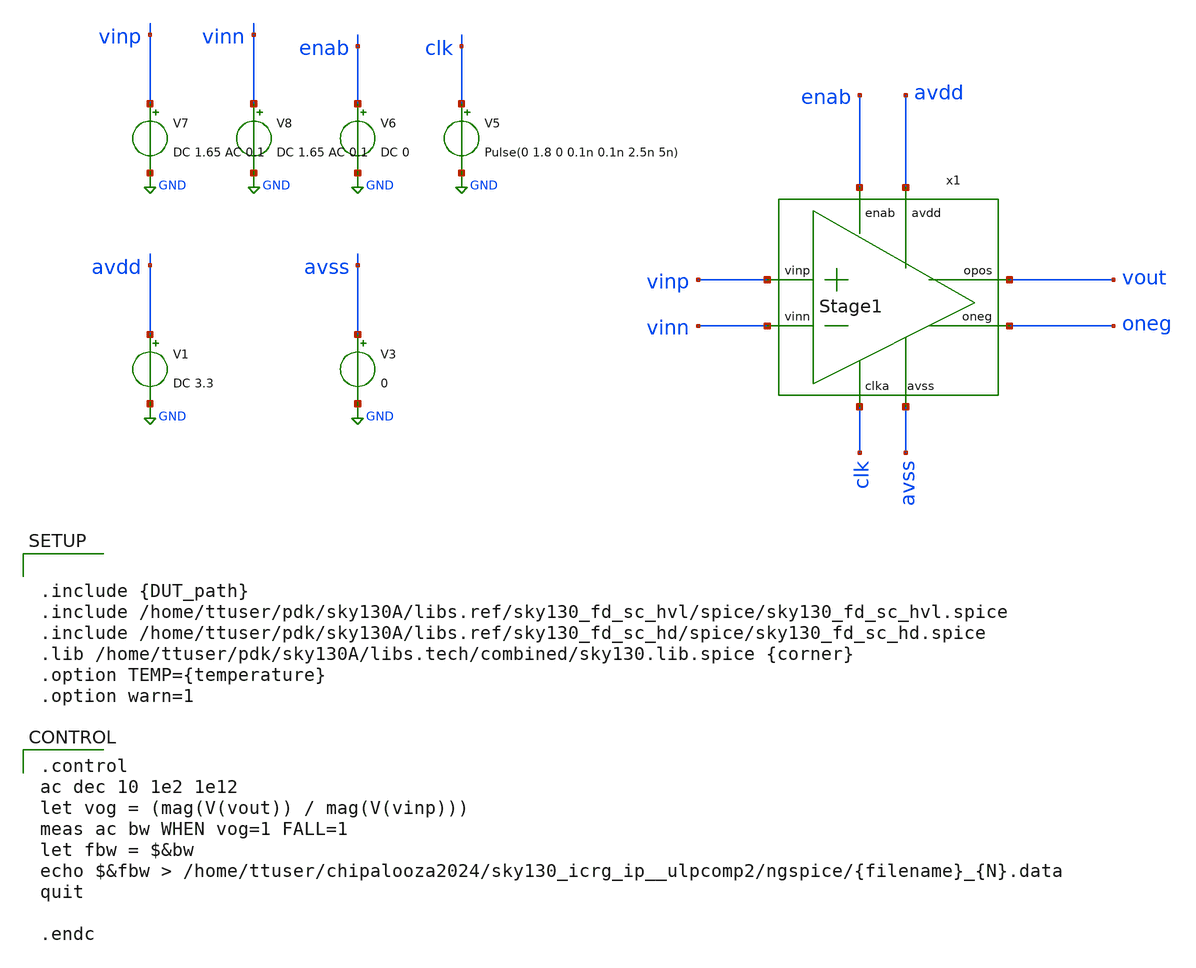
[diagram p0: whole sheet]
** sch_path: cace/fbw.sch
**.subckt fbw
V1 avdd GND DC 3.3
V3 avss GND 0
V5 clk GND Pulse(0 1.8 0 0.1n 0.1n 2.5n 5n)
V6 enab GND DC 0
V7 vinp GND DC 1.65 AC 0.1
V8 vinn GND DC 1.65 AC 0.1
x1 avdd enab clk vinn vinp oneg vout avss Stage1
**** begin user architecture code


.include {DUT_path}
.include /home/ttuser/pdk/sky130A/libs.ref/sky130_fd_sc_hvl/spice/sky130_fd_sc_hvl.spice
.include /home/ttuser/pdk/sky130A/libs.ref/sky130_fd_sc_hd/spice/sky130_fd_sc_hd.spice
.lib /home/ttuser/pdk/sky130A/libs.tech/combined/sky130.lib.spice {corner}
.option TEMP={temperature}
.option warn=1


.control
ac dec 10 1e2 1e12
let vog = (mag(V(vout)) / mag(V(vinp)))
meas ac bw WHEN vog=1 FALL=1
let fbw = $&bw
echo $&fbw > /home/ttuser/chipalooza2024/sky130_icrg_ip__ulpcomp2/ngspice/{filename}_{N}.data
quit

.endc

**** end user architecture code
**.ends

* expanding   symbol:  Stage1.sym # of pins=8
** sym_path: xschem/Stage1.sym
** sch_path: xschem/Stage1.sch
.subckt Stage1 avdd enab clka vinn vinp oneg opos avss
*.ipin avdd
*.ipin vinp
*.ipin vinn
*.opin avss
*.ipin clka
*.opin opos
*.opin oneg
*.ipin enab
XM2 oneg vinp net1 net1 sky130_fd_pr__pfet_g5v0d10v5 L=1 W=5 nf=1 ad='int((nf+1)/2) * W/nf * 0.29' as='int((nf+2)/2) * W/nf * 0.29'
+ pd='2*int((nf+1)/2) * (W/nf + 0.29)' ps='2*int((nf+2)/2) * (W/nf + 0.29)' nrd='0.29 / W' nrs='0.29 / W'
+ sa=0 sb=0 sd=0 mult=1 m=1
XM3 opos vinn net1 net1 sky130_fd_pr__pfet_g5v0d10v5 L=1 W=5 nf=1 ad='int((nf+1)/2) * W/nf * 0.29' as='int((nf+2)/2) * W/nf * 0.29'
+ pd='2*int((nf+1)/2) * (W/nf + 0.29)' ps='2*int((nf+2)/2) * (W/nf + 0.29)' nrd='0.29 / W' nrs='0.29 / W'
+ sa=0 sb=0 sd=0 mult=1 m=1
XM7 oneg clka net2 net2 sky130_fd_pr__nfet_03v3_nvt L=0.5 W=3 nf=1 ad='int((nf+1)/2) * W/nf * 0.29' as='int((nf+2)/2) * W/nf * 0.29'
+ pd='2*int((nf+1)/2) * (W/nf + 0.29)' ps='2*int((nf+2)/2) * (W/nf + 0.29)' nrd='0.29 / W' nrs='0.29 / W'
+ sa=0 sb=0 sd=0 mult=1 m=1
XM5 opos clka net2 net2 sky130_fd_pr__nfet_03v3_nvt L=0.5 W=3 nf=1 ad='int((nf+1)/2) * W/nf * 0.29' as='int((nf+2)/2) * W/nf * 0.29'
+ pd='2*int((nf+1)/2) * (W/nf + 0.29)' ps='2*int((nf+2)/2) * (W/nf + 0.29)' nrd='0.29 / W' nrs='0.29 / W'
+ sa=0 sb=0 sd=0 mult=1 m=1
XM4 net2 net2 avss avss sky130_fd_pr__nfet_03v3_nvt L=0.5 W=3 nf=1 ad='int((nf+1)/2) * W/nf * 0.29' as='int((nf+2)/2) * W/nf * 0.29'
+ pd='2*int((nf+1)/2) * (W/nf + 0.29)' ps='2*int((nf+2)/2) * (W/nf + 0.29)' nrd='0.29 / W' nrs='0.29 / W'
+ sa=0 sb=0 sd=0 mult=1 m=1
XM20 net3 enab avdd avdd sky130_fd_pr__pfet_g5v0d10v5 L=1 W=5 nf=1 ad='int((nf+1)/2) * W/nf * 0.29' as='int((nf+2)/2) * W/nf * 0.29'
+ pd='2*int((nf+1)/2) * (W/nf + 0.29)' ps='2*int((nf+2)/2) * (W/nf + 0.29)' nrd='0.29 / W' nrs='0.29 / W'
+ sa=0 sb=0 sd=0 mult=1 m=1
XM1 net1 clka net3 net3 sky130_fd_pr__pfet_g5v0d10v5 L=1 W=5 nf=1 ad='int((nf+1)/2) * W/nf * 0.29' as='int((nf+2)/2) * W/nf * 0.29'
+ pd='2*int((nf+1)/2) * (W/nf + 0.29)' ps='2*int((nf+2)/2) * (W/nf + 0.29)' nrd='0.29 / W' nrs='0.29 / W'
+ sa=0 sb=0 sd=0 mult=1 m=1
.ends

.GLOBAL GND
.end
